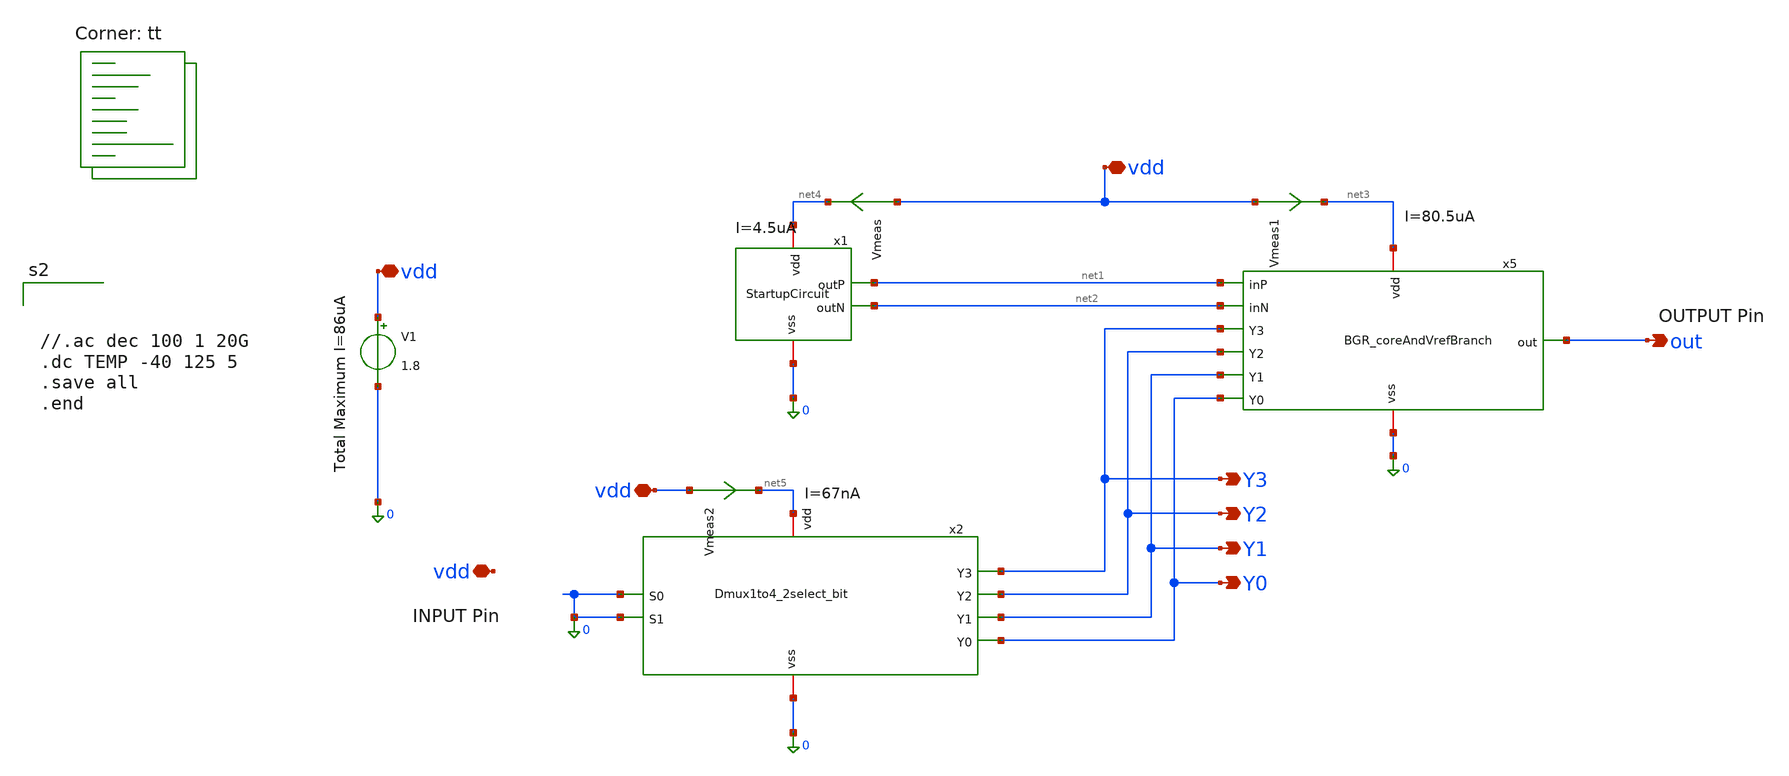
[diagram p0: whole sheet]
** sch_path: BGR_TOP_SKY130A/TB_BGR_v3.sch
**.subckt TB_BGR_v3 vdd vdd vdd vdd out Y3 Y2 Y1 Y0
*.iopin vdd
*.iopin vdd
*.iopin vdd
*.iopin vdd
*.opin out
*.opin Y3
*.opin Y2
*.opin Y1
*.opin Y0
x1 net4 net1 net2 0 StartupCircuit
V1 vdd 0 1.8
x5 net3 net1 out net2 Y3 Y2 Y1 Y0 0 BGR_coreAndVrefBranch
x2 net5 0 0 0 Y3 Y2 Y1 Y0 Dmux1to4_2select_bit
Vmeas vdd net4 0
.save i(vmeas)
Vmeas1 vdd net3 0
.save i(vmeas1)
Vmeas2 vdd net5 0
.save i(vmeas2)
**** begin user architecture code
.lib $::SKYWATER_MODELS/sky130.lib.spice tt



//.ac dec 100 1 20G
.dc TEMP -40 125 5
.save all
.end


**** end user architecture code
**.ends

* expanding   symbol:  StartupCircuit.sym # of pins=4
** sym_path: BGR_TOP_SKY130A/StartupCircuit.sym
** sch_path: BGR_TOP_SKY130A/StartupCircuit.sch
.subckt StartupCircuit vdd outP outN vss
*.iopin vdd
*.iopin vss
*.opin outP
*.opin outN
XM4 net2 outP vdd vdd sky130_fd_pr__pfet_01v8_lvt L=1 W=2 nf=1 ad='int((1 + 1)/2) * 2 / 1 * 0.29' as='int((1 + 2)/2) * 2 / 1 * 0.29'
+ pd='2*int((1 + 1)/2) * (2 / 1 + 0.29)' ps='2*int((1 + 2)/2) * (2 / 1 + 0.29)' nrd='0.29 / 2 ' nrs='0.29 / 2 '
+ sa=0 sb=0 sd=0 mult=1 m=1
XM7 outN net1 outP vdd sky130_fd_pr__pfet_01v8_lvt L=1 W=2 nf=1 ad='int((1 + 1)/2) * 2 / 1 * 0.29' as='int((1 + 2)/2) * 2 / 1 * 0.29'
+ pd='2*int((1 + 1)/2) * (2 / 1 + 0.29)' ps='2*int((1 + 2)/2) * (2 / 1 + 0.29)' nrd='0.29 / 2 ' nrs='0.29 / 2 '
+ sa=0 sb=0 sd=0 mult=2 m=2
XM9 net1 net1 net3 vss sky130_fd_pr__nfet_01v8_lvt L=1 W=1 nf=1 ad='int((1 + 1)/2) * 1 / 1 * 0.29' as='int((1 + 2)/2) * 1 / 1 * 0.29'
+ pd='2*int((1 + 1)/2) * (1 / 1 + 0.29)' ps='2*int((1 + 2)/2) * (1 / 1 + 0.29)' nrd='0.29 / 1 ' nrs='0.29 / 1 '
+ sa=0 sb=0 sd=0 mult=1 m=1
XM5 net1 outP net2 vdd sky130_fd_pr__pfet_01v8_lvt L=1 W=2 nf=1 ad='int((1 + 1)/2) * 2 / 1 * 0.29' as='int((1 + 2)/2) * 2 / 1 * 0.29'
+ pd='2*int((1 + 1)/2) * (2 / 1 + 0.29)' ps='2*int((1 + 2)/2) * (2 / 1 + 0.29)' nrd='0.29 / 2 ' nrs='0.29 / 2 '
+ sa=0 sb=0 sd=0 mult=1 m=1
XM10 net3 net3 vss vss sky130_fd_pr__nfet_01v8_lvt L=1 W=1 nf=1 ad='int((1 + 1)/2) * 1 / 1 * 0.29' as='int((1 + 2)/2) * 1 / 1 * 0.29'
+ pd='2*int((1 + 1)/2) * (1 / 1 + 0.29)' ps='2*int((1 + 2)/2) * (1 / 1 + 0.29)' nrd='0.29 / 1 ' nrs='0.29 / 1 '
+ sa=0 sb=0 sd=0 mult=1 m=1
.ends


* expanding   symbol:  BGR_coreAndVrefBranch.sym # of pins=9
** sym_path: BGR_TOP_SKY130A/BGR_coreAndVrefBranch.sym
** sch_path: BGR_TOP_SKY130A/BGR_coreAndVrefBranch.sch
.subckt BGR_coreAndVrefBranch vdd inP out inN Y3 Y2 Y1 Y0 vss
*.opin out
*.iopin vss
*.ipin Y3
*.ipin Y2
*.ipin Y1
*.ipin Y0
*.iopin vdd
*.ipin inP
*.ipin inN
XM3 out net1 vdd vdd sky130_fd_pr__pfet_01v8_lvt L=2 W=3.2 nf=1 ad='int((1 + 1)/2) * 3.2 / 1 * 0.29'
+ as='int((1 + 2)/2) * 3.2 / 1 * 0.29' pd='2*int((1 + 1)/2) * (3.2 / 1 + 0.29)' ps='2*int((1 + 2)/2) * (3.2 / 1 + 0.29)'
+ nrd='0.29 / 3.2 ' nrs='0.29 / 3.2 ' sa=0 sb=0 sd=0 mult=4 m=4
XQ3 vss vss net2 sky130_fd_pr__pnp_05v5_W3p40L3p40 m=8
XR2 net2 net4 vss sky130_fd_pr__res_high_po W=0.22 L=8 mult=1 m=1
XM11 net4 Y3 out vdd sky130_fd_pr__pfet_01v8_lvt L=1 W=5 nf=1 ad='int((1 + 1)/2) * 5 / 1 * 0.29' as='int((1 + 2)/2) * 5 / 1 * 0.29'
+ pd='2*int((1 + 1)/2) * (5 / 1 + 0.29)' ps='2*int((1 + 2)/2) * (5 / 1 + 0.29)' nrd='0.29 / 5 ' nrs='0.29 / 5 '
+ sa=0 sb=0 sd=0 mult=8 m=8
XM12 net4 Y2 net5 vdd sky130_fd_pr__pfet_01v8_lvt L=1 W=5 nf=1 ad='int((1 + 1)/2) * 5 / 1 * 0.29' as='int((1 + 2)/2) * 5 / 1 * 0.29'
+ pd='2*int((1 + 1)/2) * (5 / 1 + 0.29)' ps='2*int((1 + 2)/2) * (5 / 1 + 0.29)' nrd='0.29 / 5 ' nrs='0.29 / 5 '
+ sa=0 sb=0 sd=0 mult=8 m=8
XM13 net4 Y1 net6 vdd sky130_fd_pr__pfet_01v8_lvt L=1 W=5 nf=1 ad='int((1 + 1)/2) * 5 / 1 * 0.29' as='int((1 + 2)/2) * 5 / 1 * 0.29'
+ pd='2*int((1 + 1)/2) * (5 / 1 + 0.29)' ps='2*int((1 + 2)/2) * (5 / 1 + 0.29)' nrd='0.29 / 5 ' nrs='0.29 / 5 '
+ sa=0 sb=0 sd=0 mult=8 m=8
XM14 net4 Y0 net3 vdd sky130_fd_pr__pfet_01v8_lvt L=1 W=5 nf=1 ad='int((1 + 1)/2) * 5 / 1 * 0.29' as='int((1 + 2)/2) * 5 / 1 * 0.29'
+ pd='2*int((1 + 1)/2) * (5 / 1 + 0.29)' ps='2*int((1 + 2)/2) * (5 / 1 + 0.29)' nrd='0.29 / 5 ' nrs='0.29 / 5 '
+ sa=0 sb=0 sd=0 mult=8 m=8
XR1 net3 net6 vss sky130_fd_pr__res_high_po W=1 L=0.5 mult=1 m=1
XR3 net6 net5 vss sky130_fd_pr__res_high_po W=2.304 L=0.5 mult=1 m=1
XR4 net5 out vss sky130_fd_pr__res_high_po W=2.147 L=0.5 mult=1 m=1
XM6 inN inN net9 vss sky130_fd_pr__nfet_01v8_lvt L=1 W=3.8 nf=1 ad='int((1 + 1)/2) * 3.8 / 1 * 0.29'
+ as='int((1 + 2)/2) * 3.8 / 1 * 0.29' pd='2*int((1 + 1)/2) * (3.8 / 1 + 0.29)' ps='2*int((1 + 2)/2) * (3.8 / 1 + 0.29)'
+ nrd='0.29 / 3.8 ' nrs='0.29 / 3.8 ' sa=0 sb=0 sd=0 mult=8 m=8
XM1 inN inP vdd vdd sky130_fd_pr__pfet_01v8_lvt L=2 W=3.2 nf=1 ad='int((1 + 1)/2) * 3.2 / 1 * 0.29' as='int((1 + 2)/2) * 3.2 / 1 * 0.29'
+ pd='2*int((1 + 1)/2) * (3.2 / 1 + 0.29)' ps='2*int((1 + 2)/2) * (3.2 / 1 + 0.29)' nrd='0.29 / 3.2 ' nrs='0.29 / 3.2 '
+ sa=0 sb=0 sd=0 mult=4 m=4
XQ1 vss vss net8 sky130_fd_pr__pnp_05v5_W3p40L3p40 m=8
XR5 net8 net7 vss sky130_fd_pr__res_high_po W=1.1 L=14.6 mult=1 m=1
XM2 net1 net1 vdd vdd sky130_fd_pr__pfet_01v8_lvt L=2 W=3.2 nf=1 ad='int((1 + 1)/2) * 3.2 / 1 * 0.29'
+ as='int((1 + 2)/2) * 3.2 / 1 * 0.29' pd='2*int((1 + 1)/2) * (3.2 / 1 + 0.29)' ps='2*int((1 + 2)/2) * (3.2 / 1 + 0.29)'
+ nrd='0.29 / 3.2 ' nrs='0.29 / 3.2 ' sa=0 sb=0 sd=0 mult=4 m=4
XM8 net1 inN net7 vss sky130_fd_pr__nfet_01v8_lvt L=1 W=3.8 nf=1 ad='int((1 + 1)/2) * 3.8 / 1 * 0.29'
+ as='int((1 + 2)/2) * 3.8 / 1 * 0.29' pd='2*int((1 + 1)/2) * (3.8 / 1 + 0.29)' ps='2*int((1 + 2)/2) * (3.8 / 1 + 0.29)'
+ nrd='0.29 / 3.8 ' nrs='0.29 / 3.8 ' sa=0 sb=0 sd=0 mult=8 m=8
XQ2 vss vss net10 sky130_fd_pr__pnp_05v5_W3p40L3p40 m=1
XR6 net10 net9 vss sky130_fd_pr__res_high_po W=2.28 L=14.6 mult=1 m=1
XR7 net1 inP vss sky130_fd_pr__res_high_po W=2000 L=0.01 mult=1000 m=1000
.ends


* expanding   symbol:  Dmux1to4_2select_bit.sym # of pins=8
** sym_path: BGR_TOP_SKY130A/Dmux1to4_2select_bit.sym
** sch_path: BGR_TOP_SKY130A/Dmux1to4_2select_bit.sch
.subckt Dmux1to4_2select_bit vdd S0 S1 vss Y3 Y2 Y1 Y0
*.ipin S0
*.ipin S1
*.iopin vdd
*.iopin vss
*.opin Y3
*.opin Y2
*.opin Y1
*.opin Y0
x1 vdd Y3 vdd S0 S1 vss NAND
x2 vdd S1 net2 vss NOT
x3 vdd S0 net1 vss NOT
x4 vdd Y2 vdd net1 S1 vss NAND
x5 vdd Y1 vdd S0 net2 vss NAND
x6 vdd Y0 vdd net1 net2 vss NAND
.ends


* expanding   symbol:  NAND.sym # of pins=6
** sym_path: BGR_TOP_SKY130A/NAND.sym
** sch_path: BGR_TOP_SKY130A/NAND.sch
.subckt NAND vdd out A B C vss
*.iopin vdd
*.iopin vss
*.ipin A
*.ipin C
*.ipin B
*.opin out
XM6 out A net1 vss sky130_fd_pr__nfet_01v8_lvt L=1 W=1 nf=1 ad='int((1 + 1)/2) * 1 / 1 * 0.29' as='int((1 + 2)/2) * 1 / 1 * 0.29'
+ pd='2*int((1 + 1)/2) * (1 / 1 + 0.29)' ps='2*int((1 + 2)/2) * (1 / 1 + 0.29)' nrd='0.29 / 1 ' nrs='0.29 / 1 '
+ sa=0 sb=0 sd=0 mult=2 m=2
XM1 out B vdd vdd sky130_fd_pr__pfet_01v8_lvt L=1 W=1 nf=1 ad='int((1 + 1)/2) * 1 / 1 * 0.29' as='int((1 + 2)/2) * 1 / 1 * 0.29'
+ pd='2*int((1 + 1)/2) * (1 / 1 + 0.29)' ps='2*int((1 + 2)/2) * (1 / 1 + 0.29)' nrd='0.29 / 1 ' nrs='0.29 / 1 '
+ sa=0 sb=0 sd=0 mult=4 m=4
XM2 out A vdd vdd sky130_fd_pr__pfet_01v8_lvt L=1 W=1 nf=1 ad='int((1 + 1)/2) * 1 / 1 * 0.29' as='int((1 + 2)/2) * 1 / 1 * 0.29'
+ pd='2*int((1 + 1)/2) * (1 / 1 + 0.29)' ps='2*int((1 + 2)/2) * (1 / 1 + 0.29)' nrd='0.29 / 1 ' nrs='0.29 / 1 '
+ sa=0 sb=0 sd=0 mult=4 m=4
XM3 net1 B net2 vss sky130_fd_pr__nfet_01v8_lvt L=1 W=1 nf=1 ad='int((1 + 1)/2) * 1 / 1 * 0.29' as='int((1 + 2)/2) * 1 / 1 * 0.29'
+ pd='2*int((1 + 1)/2) * (1 / 1 + 0.29)' ps='2*int((1 + 2)/2) * (1 / 1 + 0.29)' nrd='0.29 / 1 ' nrs='0.29 / 1 '
+ sa=0 sb=0 sd=0 mult=2 m=2
XM4 out C vdd vdd sky130_fd_pr__pfet_01v8_lvt L=1 W=1 nf=1 ad='int((1 + 1)/2) * 1 / 1 * 0.29' as='int((1 + 2)/2) * 1 / 1 * 0.29'
+ pd='2*int((1 + 1)/2) * (1 / 1 + 0.29)' ps='2*int((1 + 2)/2) * (1 / 1 + 0.29)' nrd='0.29 / 1 ' nrs='0.29 / 1 '
+ sa=0 sb=0 sd=0 mult=4 m=4
XM5 net2 C vss vss sky130_fd_pr__nfet_01v8_lvt L=1 W=1 nf=1 ad='int((1 + 1)/2) * 1 / 1 * 0.29' as='int((1 + 2)/2) * 1 / 1 * 0.29'
+ pd='2*int((1 + 1)/2) * (1 / 1 + 0.29)' ps='2*int((1 + 2)/2) * (1 / 1 + 0.29)' nrd='0.29 / 1 ' nrs='0.29 / 1 '
+ sa=0 sb=0 sd=0 mult=2 m=2
.ends


* expanding   symbol:  NOT.sym # of pins=4
** sym_path: BGR_TOP_SKY130A/NOT.sym
** sch_path: BGR_TOP_SKY130A/NOT.sch
.subckt NOT vdd in out vss
*.iopin vdd
*.iopin vss
*.ipin in
*.opin out
XM6 out in vss vss sky130_fd_pr__nfet_01v8_lvt L=1 W=1 nf=1 ad='int((1 + 1)/2) * 1 / 1 * 0.29' as='int((1 + 2)/2) * 1 / 1 * 0.29'
+ pd='2*int((1 + 1)/2) * (1 / 1 + 0.29)' ps='2*int((1 + 2)/2) * (1 / 1 + 0.29)' nrd='0.29 / 1 ' nrs='0.29 / 1 '
+ sa=0 sb=0 sd=0 mult=1 m=1
XM1 out in vdd vdd sky130_fd_pr__pfet_01v8_lvt L=1 W=1 nf=1 ad='int((1 + 1)/2) * 1 / 1 * 0.29' as='int((1 + 2)/2) * 1 / 1 * 0.29'
+ pd='2*int((1 + 1)/2) * (1 / 1 + 0.29)' ps='2*int((1 + 2)/2) * (1 / 1 + 0.29)' nrd='0.29 / 1 ' nrs='0.29 / 1 '
+ sa=0 sb=0 sd=0 mult=2 m=2
.ends

.end
